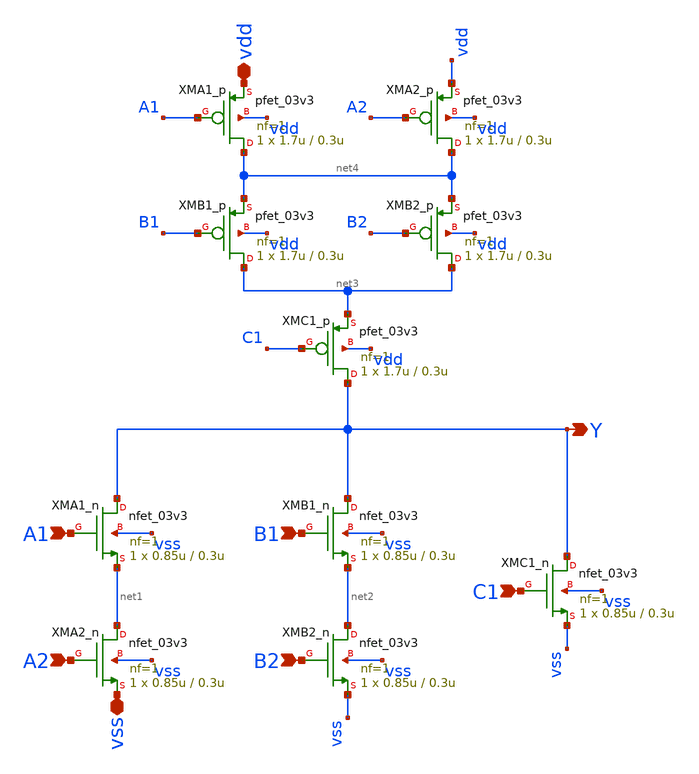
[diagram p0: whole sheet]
** sch_path: designs/aoi221/alternative/gf180mcu_gp9t3v3__aoi221_1.sch
**.subckt gf180mcu_gp9t3v3__aoi221_1 vdd vss A1 A2 B2 B1 C1 Y
*.iopin vdd
*.iopin vss
*.ipin A1
*.ipin A2
*.ipin B2
*.ipin B1
*.ipin C1
*.opin Y
XMA1_n Y A1 net1 vss nfet_03v3 L=0.3u W=0.85u nf=1 ad='int((nf+1)/2) * W/nf * 0.18u' as='int((nf+2)/2) * W/nf * 0.18u'
+ pd='2*int((nf+1)/2) * (W/nf + 0.18u)' ps='2*int((nf+2)/2) * (W/nf + 0.18u)' nrd='0.18u / W' nrs='0.18u / W'
+ sa=0 sb=0 sd=0 m=1
XMA2_n net1 A2 vss vss nfet_03v3 L=0.3u W=0.85u nf=1 ad='int((nf+1)/2) * W/nf * 0.18u' as='int((nf+2)/2) * W/nf * 0.18u'
+ pd='2*int((nf+1)/2) * (W/nf + 0.18u)' ps='2*int((nf+2)/2) * (W/nf + 0.18u)' nrd='0.18u / W' nrs='0.18u / W'
+ sa=0 sb=0 sd=0 m=1
XMB1_n Y B1 net2 vss nfet_03v3 L=0.3u W=0.85u nf=1 ad='int((nf+1)/2) * W/nf * 0.18u' as='int((nf+2)/2) * W/nf * 0.18u'
+ pd='2*int((nf+1)/2) * (W/nf + 0.18u)' ps='2*int((nf+2)/2) * (W/nf + 0.18u)' nrd='0.18u / W' nrs='0.18u / W'
+ sa=0 sb=0 sd=0 m=1
XMB2_n net2 B2 vss vss nfet_03v3 L=0.3u W=0.85u nf=1 ad='int((nf+1)/2) * W/nf * 0.18u' as='int((nf+2)/2) * W/nf * 0.18u'
+ pd='2*int((nf+1)/2) * (W/nf + 0.18u)' ps='2*int((nf+2)/2) * (W/nf + 0.18u)' nrd='0.18u / W' nrs='0.18u / W'
+ sa=0 sb=0 sd=0 m=1
XMC1_n Y C1 vss vss nfet_03v3 L=0.3u W=0.85u nf=1 ad='int((nf+1)/2) * W/nf * 0.18u' as='int((nf+2)/2) * W/nf * 0.18u'
+ pd='2*int((nf+1)/2) * (W/nf + 0.18u)' ps='2*int((nf+2)/2) * (W/nf + 0.18u)' nrd='0.18u / W' nrs='0.18u / W'
+ sa=0 sb=0 sd=0 m=1
XMA1_p net4 A1 vdd vdd pfet_03v3 L=0.3u W=1.7u nf=1 ad='int((nf+1)/2) * W/nf * 0.18u' as='int((nf+2)/2) * W/nf * 0.18u'
+ pd='2*int((nf+1)/2) * (W/nf + 0.18u)' ps='2*int((nf+2)/2) * (W/nf + 0.18u)' nrd='0.18u / W' nrs='0.18u / W'
+ sa=0 sb=0 sd=0 m=1
XMA2_p net4 A2 vdd vdd pfet_03v3 L=0.3u W=1.7u nf=1 ad='int((nf+1)/2) * W/nf * 0.18u' as='int((nf+2)/2) * W/nf * 0.18u'
+ pd='2*int((nf+1)/2) * (W/nf + 0.18u)' ps='2*int((nf+2)/2) * (W/nf + 0.18u)' nrd='0.18u / W' nrs='0.18u / W'
+ sa=0 sb=0 sd=0 m=1
XMB1_p net3 B1 net4 vdd pfet_03v3 L=0.3u W=1.7u nf=1 ad='int((nf+1)/2) * W/nf * 0.18u' as='int((nf+2)/2) * W/nf * 0.18u'
+ pd='2*int((nf+1)/2) * (W/nf + 0.18u)' ps='2*int((nf+2)/2) * (W/nf + 0.18u)' nrd='0.18u / W' nrs='0.18u / W'
+ sa=0 sb=0 sd=0 m=1
XMB2_p net3 B2 net4 vdd pfet_03v3 L=0.3u W=1.7u nf=1 ad='int((nf+1)/2) * W/nf * 0.18u' as='int((nf+2)/2) * W/nf * 0.18u'
+ pd='2*int((nf+1)/2) * (W/nf + 0.18u)' ps='2*int((nf+2)/2) * (W/nf + 0.18u)' nrd='0.18u / W' nrs='0.18u / W'
+ sa=0 sb=0 sd=0 m=1
XMC1_p Y C1 net3 vdd pfet_03v3 L=0.3u W=1.7u nf=1 ad='int((nf+1)/2) * W/nf * 0.18u' as='int((nf+2)/2) * W/nf * 0.18u'
+ pd='2*int((nf+1)/2) * (W/nf + 0.18u)' ps='2*int((nf+2)/2) * (W/nf + 0.18u)' nrd='0.18u / W' nrs='0.18u / W'
+ sa=0 sb=0 sd=0 m=1
**.ends
.end
